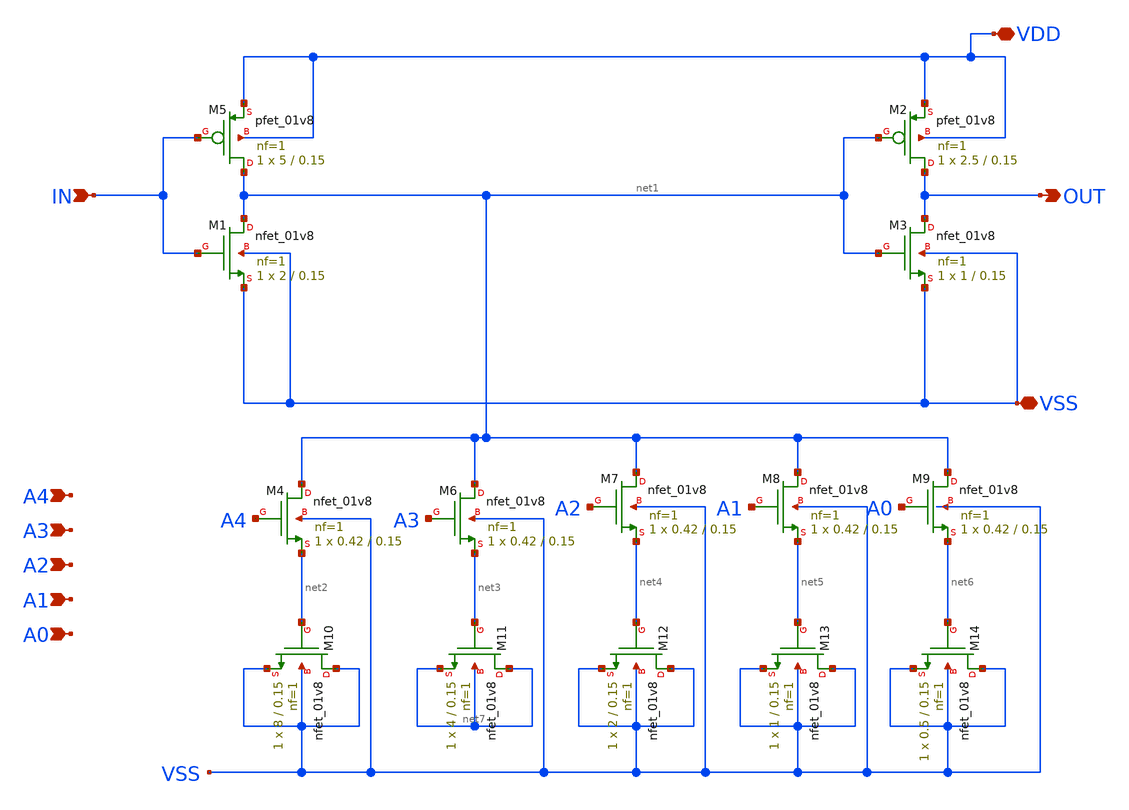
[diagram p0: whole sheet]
** sch_path: xschem/schematic/SCI_DCDL/mos_capacitive_baseline/SCI_1bit.sch
**.subckt SCI_1bit IN OUT VDD VSS A4 A3 A2 A1 A0
*.ipin IN
*.opin OUT
*.iopin VDD
*.iopin VSS
*.ipin A4
*.ipin A3
*.ipin A2
*.ipin A1
*.ipin A0
XM1 net1 IN VSS VSS sky130_fd_pr__nfet_01v8 L=0.15 W=2 nf=1 ad='int((1 + 1)/2) * 2 / 1 * 0.29' as='int((1 + 2)/2) * 2 / 1 * 0.29'
+ pd='2*int((1 + 1)/2) * (2 / 1 + 0.29)' ps='2*int((1 + 2)/2) * (2 / 1 + 0.29)' nrd='0.29 / 2 ' nrs='0.29 / 2 '
+ sa=0 sb=0 sd=0 mult=1 m=1
XM3 OUT net1 VSS VSS sky130_fd_pr__nfet_01v8 L=0.15 W=1 nf=1 ad='int((1 + 1)/2) * 1 / 1 * 0.29' as='int((1 + 2)/2) * 1 / 1 * 0.29'
+ pd='2*int((1 + 1)/2) * (1 / 1 + 0.29)' ps='2*int((1 + 2)/2) * (1 / 1 + 0.29)' nrd='0.29 / 1 ' nrs='0.29 / 1 '
+ sa=0 sb=0 sd=0 mult=1 m=1
XM5 net1 IN VDD VDD sky130_fd_pr__pfet_01v8 L=0.15 W=5 nf=1 ad='int((1 + 1)/2) * 5 / 1 * 0.29' as='int((1 + 2)/2) * 5 / 1 * 0.29'
+ pd='2*int((1 + 1)/2) * (5 / 1 + 0.29)' ps='2*int((1 + 2)/2) * (5 / 1 + 0.29)' nrd='0.29 / 5 ' nrs='0.29 / 5 '
+ sa=0 sb=0 sd=0 mult=1 m=1
XM2 OUT net1 VDD VDD sky130_fd_pr__pfet_01v8 L=0.15 W=2.5 nf=1 ad='int((1 + 1)/2) * 2.5 / 1 * 0.29' as='int((1 + 2)/2) * 2.5 / 1 * 0.29'
+ pd='2*int((1 + 1)/2) * (2.5 / 1 + 0.29)' ps='2*int((1 + 2)/2) * (2.5 / 1 + 0.29)' nrd='0.29 / 2.5 ' nrs='0.29 / 2.5 '
+ sa=0 sb=0 sd=0 mult=1 m=1
XM4 net1 A4 net2 VSS sky130_fd_pr__nfet_01v8 L=0.15 W=0.42 nf=1 ad='int((1 + 1)/2) * 0.42 / 1 * 0.29'
+ as='int((1 + 2)/2) * 0.42 / 1 * 0.29' pd='2*int((1 + 1)/2) * (0.42 / 1 + 0.29)' ps='2*int((1 + 2)/2) * (0.42 / 1 + 0.29)'
+ nrd='0.29 / 0.42 ' nrs='0.29 / 0.42 ' sa=0 sb=0 sd=0 mult=1 m=1
XM6 net1 A3 net3 VSS sky130_fd_pr__nfet_01v8 L=0.15 W=0.42 nf=1 ad='int((1 + 1)/2) * 0.42 / 1 * 0.29'
+ as='int((1 + 2)/2) * 0.42 / 1 * 0.29' pd='2*int((1 + 1)/2) * (0.42 / 1 + 0.29)' ps='2*int((1 + 2)/2) * (0.42 / 1 + 0.29)'
+ nrd='0.29 / 0.42 ' nrs='0.29 / 0.42 ' sa=0 sb=0 sd=0 mult=1 m=1
XM7 net1 A2 net4 VSS sky130_fd_pr__nfet_01v8 L=0.15 W=0.42 nf=1 ad='int((1 + 1)/2) * 0.42 / 1 * 0.29'
+ as='int((1 + 2)/2) * 0.42 / 1 * 0.29' pd='2*int((1 + 1)/2) * (0.42 / 1 + 0.29)' ps='2*int((1 + 2)/2) * (0.42 / 1 + 0.29)'
+ nrd='0.29 / 0.42 ' nrs='0.29 / 0.42 ' sa=0 sb=0 sd=0 mult=1 m=1
XM8 net1 A1 net5 VSS sky130_fd_pr__nfet_01v8 L=0.15 W=0.42 nf=1 ad='int((1 + 1)/2) * 0.42 / 1 * 0.29'
+ as='int((1 + 2)/2) * 0.42 / 1 * 0.29' pd='2*int((1 + 1)/2) * (0.42 / 1 + 0.29)' ps='2*int((1 + 2)/2) * (0.42 / 1 + 0.29)'
+ nrd='0.29 / 0.42 ' nrs='0.29 / 0.42 ' sa=0 sb=0 sd=0 mult=1 m=1
XM9 net1 A0 net6 VSS sky130_fd_pr__nfet_01v8 L=0.15 W=0.42 nf=1 ad='int((1 + 1)/2) * 0.42 / 1 * 0.29'
+ as='int((1 + 2)/2) * 0.42 / 1 * 0.29' pd='2*int((1 + 1)/2) * (0.42 / 1 + 0.29)' ps='2*int((1 + 2)/2) * (0.42 / 1 + 0.29)'
+ nrd='0.29 / 0.42 ' nrs='0.29 / 0.42 ' sa=0 sb=0 sd=0 mult=1 m=1
XM10 VSS net2 VSS VSS sky130_fd_pr__nfet_01v8 L=0.15 W=8 nf=1 ad='int((1 + 1)/2) * 8 / 1 * 0.29' as='int((1 + 2)/2) * 8 / 1 * 0.29'
+ pd='2*int((1 + 1)/2) * (8 / 1 + 0.29)' ps='2*int((1 + 2)/2) * (8 / 1 + 0.29)' nrd='0.29 / 8 ' nrs='0.29 / 8 '
+ sa=0 sb=0 sd=0 mult=1 m=1
XM11 net7 net3 net7 net7 sky130_fd_pr__nfet_01v8 L=0.15 W=4 nf=1 ad='int((1 + 1)/2) * 4 / 1 * 0.29' as='int((1 + 2)/2) * 4 / 1 * 0.29'
+ pd='2*int((1 + 1)/2) * (4 / 1 + 0.29)' ps='2*int((1 + 2)/2) * (4 / 1 + 0.29)' nrd='0.29 / 4 ' nrs='0.29 / 4 '
+ sa=0 sb=0 sd=0 mult=1 m=1
XM12 VSS net4 VSS VSS sky130_fd_pr__nfet_01v8 L=0.15 W=2 nf=1 ad='int((1 + 1)/2) * 2 / 1 * 0.29' as='int((1 + 2)/2) * 2 / 1 * 0.29'
+ pd='2*int((1 + 1)/2) * (2 / 1 + 0.29)' ps='2*int((1 + 2)/2) * (2 / 1 + 0.29)' nrd='0.29 / 2 ' nrs='0.29 / 2 '
+ sa=0 sb=0 sd=0 mult=1 m=1
XM13 VSS net5 VSS VSS sky130_fd_pr__nfet_01v8 L=0.15 W=1 nf=1 ad='int((1 + 1)/2) * 1 / 1 * 0.29' as='int((1 + 2)/2) * 1 / 1 * 0.29'
+ pd='2*int((1 + 1)/2) * (1 / 1 + 0.29)' ps='2*int((1 + 2)/2) * (1 / 1 + 0.29)' nrd='0.29 / 1 ' nrs='0.29 / 1 '
+ sa=0 sb=0 sd=0 mult=1 m=1
XM14 VSS net6 VSS VSS sky130_fd_pr__nfet_01v8 L=0.15 W=0.5 nf=1 ad='int((1 + 1)/2) * 0.5 / 1 * 0.29'
+ as='int((1 + 2)/2) * 0.5 / 1 * 0.29' pd='2*int((1 + 1)/2) * (0.5 / 1 + 0.29)' ps='2*int((1 + 2)/2) * (0.5 / 1 + 0.29)'
+ nrd='0.29 / 0.5 ' nrs='0.29 / 0.5 ' sa=0 sb=0 sd=0 mult=1 m=1
**.ends
.end
